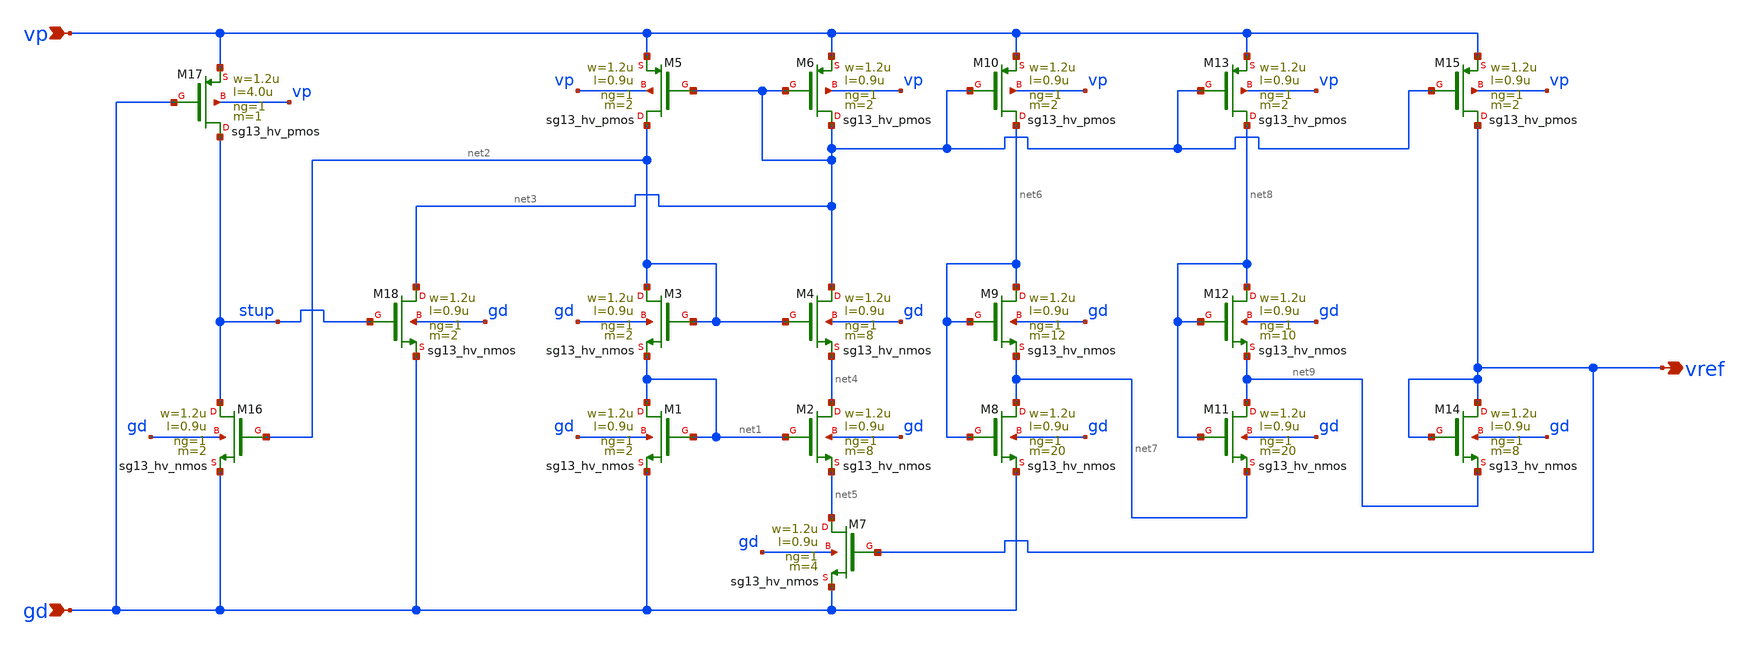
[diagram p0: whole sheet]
** sch_path: circuit/bandgap_selfbias_core.sch
**.subckt bandgap_selfbias_core gd vp vref
*.ipin gd
*.ipin vp
*.opin vref
XM1 net1 net1 gd gd sg13_hv_nmos w=1.2u l=0.9u ng=1 m=2 mm_ok=1
XM2 net4 net1 net5 gd sg13_hv_nmos w=1.2u l=0.9u ng=1 m=8 mm_ok=1
XM7 net5 vref gd gd sg13_hv_nmos w=1.2u l=0.9u ng=1 m=4 mm_ok=1
XM3 net2 net2 net1 gd sg13_hv_nmos w=1.2u l=0.9u ng=1 m=2 mm_ok=1
XM4 net3 net2 net4 gd sg13_hv_nmos w=1.2u l=0.9u ng=1 m=8 mm_ok=1
XM6 net3 net3 vp vp sg13_hv_pmos w=1.2u l=0.9u ng=1 m=2 mm_ok=1
XM5 net2 net3 vp vp sg13_hv_pmos w=1.2u l=0.9u ng=1 m=2 mm_ok=1
XM10 net6 net3 vp vp sg13_hv_pmos w=1.2u l=0.9u ng=1 m=2 mm_ok=1
XM8 net7 net6 gd gd sg13_hv_nmos w=1.2u l=0.9u ng=1 m=20 mm_ok=1
XM9 net6 net6 net7 gd sg13_hv_nmos w=1.2u l=0.9u ng=1 m=12 mm_ok=1
XM13 net8 net3 vp vp sg13_hv_pmos w=1.2u l=0.9u ng=1 m=2 mm_ok=1
XM11 net9 net8 net7 gd sg13_hv_nmos w=1.2u l=0.9u ng=1 m=20 mm_ok=1
XM12 net8 net8 net9 gd sg13_hv_nmos w=1.2u l=0.9u ng=1 m=10 mm_ok=1
XM14 vref vref net9 gd sg13_hv_nmos w=1.2u l=0.9u ng=1 m=8 mm_ok=1
XM15 vref net3 vp vp sg13_hv_pmos w=1.2u l=0.9u ng=1 m=2 mm_ok=1
XM16 stup net2 gd gd sg13_hv_nmos w=1.2u l=0.9u ng=1 m=2 mm_ok=1
XM17 stup gd vp vp sg13_hv_pmos w=1.2u l=4.0u ng=1 m=1 mm_ok=1
XM18 net3 stup gd gd sg13_hv_nmos w=1.2u l=0.9u ng=1 m=2 mm_ok=1
**.ends
.end
